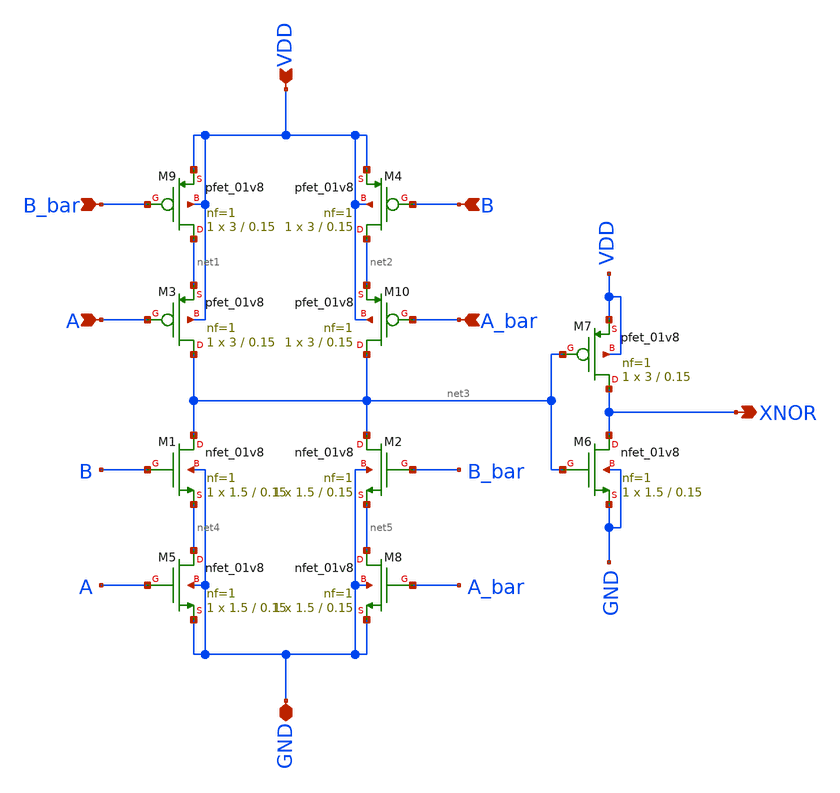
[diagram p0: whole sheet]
** sch_path: skywater_stuff/CMOS_XNOR.sch
**.subckt CMOS_XNOR A A_bar B B_bar XNOR GND VDD
*.ipin A
*.ipin A_bar
*.ipin B
*.ipin B_bar
*.opin XNOR
*.iopin GND
*.ipin VDD
XM8 net5 A_bar GND GND sky130_fd_pr__nfet_01v8 L=0.15 W=1.5 nf=1 ad='int((nf+1)/2) * W/nf * 0.29' as='int((nf+2)/2) * W/nf * 0.29'
+ pd='2*int((nf+1)/2) * (W/nf + 0.29)' ps='2*int((nf+2)/2) * (W/nf + 0.29)' nrd='0.29 / W' nrs='0.29 / W'
+ sa=0 sb=0 sd=0 mult=1 m=1
XM1 net3 B net4 GND sky130_fd_pr__nfet_01v8 L=0.15 W=1.5 nf=1 ad='int((nf+1)/2) * W/nf * 0.29' as='int((nf+2)/2) * W/nf * 0.29'
+ pd='2*int((nf+1)/2) * (W/nf + 0.29)' ps='2*int((nf+2)/2) * (W/nf + 0.29)' nrd='0.29 / W' nrs='0.29 / W'
+ sa=0 sb=0 sd=0 mult=1 m=1
XM3 net3 A net1 VDD sky130_fd_pr__pfet_01v8 L=0.15 W=3 nf=1 ad='int((nf+1)/2) * W/nf * 0.29' as='int((nf+2)/2) * W/nf * 0.29'
+ pd='2*int((nf+1)/2) * (W/nf + 0.29)' ps='2*int((nf+2)/2) * (W/nf + 0.29)' nrd='0.29 / W' nrs='0.29 / W'
+ sa=0 sb=0 sd=0 mult=1 m=1
XM4 net2 B VDD VDD sky130_fd_pr__pfet_01v8 L=0.15 W=3 nf=1 ad='int((nf+1)/2) * W/nf * 0.29' as='int((nf+2)/2) * W/nf * 0.29'
+ pd='2*int((nf+1)/2) * (W/nf + 0.29)' ps='2*int((nf+2)/2) * (W/nf + 0.29)' nrd='0.29 / W' nrs='0.29 / W'
+ sa=0 sb=0 sd=0 mult=1 m=1
XM9 net1 B_bar VDD VDD sky130_fd_pr__pfet_01v8 L=0.15 W=3 nf=1 ad='int((nf+1)/2) * W/nf * 0.29' as='int((nf+2)/2) * W/nf * 0.29'
+ pd='2*int((nf+1)/2) * (W/nf + 0.29)' ps='2*int((nf+2)/2) * (W/nf + 0.29)' nrd='0.29 / W' nrs='0.29 / W'
+ sa=0 sb=0 sd=0 mult=1 m=1
XM2 net3 B_bar net5 GND sky130_fd_pr__nfet_01v8 L=0.15 W=1.5 nf=1 ad='int((nf+1)/2) * W/nf * 0.29' as='int((nf+2)/2) * W/nf * 0.29'
+ pd='2*int((nf+1)/2) * (W/nf + 0.29)' ps='2*int((nf+2)/2) * (W/nf + 0.29)' nrd='0.29 / W' nrs='0.29 / W'
+ sa=0 sb=0 sd=0 mult=1 m=1
XM5 net4 A GND GND sky130_fd_pr__nfet_01v8 L=0.15 W=1.5 nf=1 ad='int((nf+1)/2) * W/nf * 0.29' as='int((nf+2)/2) * W/nf * 0.29'
+ pd='2*int((nf+1)/2) * (W/nf + 0.29)' ps='2*int((nf+2)/2) * (W/nf + 0.29)' nrd='0.29 / W' nrs='0.29 / W'
+ sa=0 sb=0 sd=0 mult=1 m=1
XM10 net3 A_bar net2 VDD sky130_fd_pr__pfet_01v8 L=0.15 W=3 nf=1 ad='int((nf+1)/2) * W/nf * 0.29' as='int((nf+2)/2) * W/nf * 0.29'
+ pd='2*int((nf+1)/2) * (W/nf + 0.29)' ps='2*int((nf+2)/2) * (W/nf + 0.29)' nrd='0.29 / W' nrs='0.29 / W'
+ sa=0 sb=0 sd=0 mult=1 m=1
XM6 XNOR net3 GND GND sky130_fd_pr__nfet_01v8 L=0.15 W=1.5 nf=1 ad='int((nf+1)/2) * W/nf * 0.29' as='int((nf+2)/2) * W/nf * 0.29'
+ pd='2*int((nf+1)/2) * (W/nf + 0.29)' ps='2*int((nf+2)/2) * (W/nf + 0.29)' nrd='0.29 / W' nrs='0.29 / W'
+ sa=0 sb=0 sd=0 mult=1 m=1
XM7 XNOR net3 VDD VDD sky130_fd_pr__pfet_01v8 L=0.15 W=3 nf=1 ad='int((nf+1)/2) * W/nf * 0.29' as='int((nf+2)/2) * W/nf * 0.29'
+ pd='2*int((nf+1)/2) * (W/nf + 0.29)' ps='2*int((nf+2)/2) * (W/nf + 0.29)' nrd='0.29 / W' nrs='0.29 / W'
+ sa=0 sb=0 sd=0 mult=1 m=1
**.ends
.end
